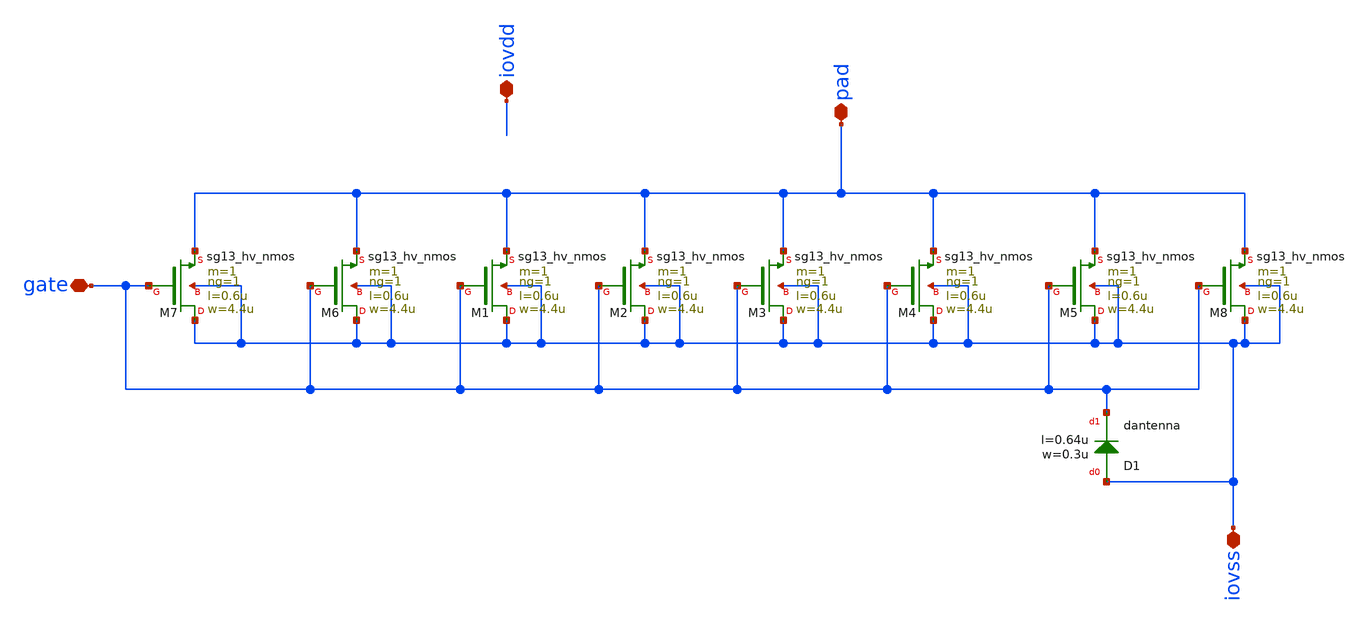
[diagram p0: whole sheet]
** sch_path: ihp-sg13g2/libs.ref/sg13g2_io/xschem/sg13g2_Clamp_N8N8D.sch
**.subckt sg13g2_Clamp_N8N8D iovss pad gate iovdd
*.iopin iovss
*.iopin pad
*.iopin gate
*.iopin iovdd
XM1 iovss gate pad iovss sg13_hv_nmos w=4.4u l=0.6u ng=1 m=1 mm_ok=1
XM2 iovss gate pad iovss sg13_hv_nmos w=4.4u l=0.6u ng=1 m=1 mm_ok=1
XM3 iovss gate pad iovss sg13_hv_nmos w=4.4u l=0.6u ng=1 m=1 mm_ok=1
XM4 iovss gate pad iovss sg13_hv_nmos w=4.4u l=0.6u ng=1 m=1 mm_ok=1
XM5 iovss gate pad iovss sg13_hv_nmos w=4.4u l=0.6u ng=1 m=1 mm_ok=1
XM6 iovss gate pad iovss sg13_hv_nmos w=4.4u l=0.6u ng=1 m=1 mm_ok=1
XM7 iovss gate pad iovss sg13_hv_nmos w=4.4u l=0.6u ng=1 m=1 mm_ok=1
XM8 iovss gate pad iovss sg13_hv_nmos w=4.4u l=0.6u ng=1 m=1 mm_ok=1
XD1 iovss gate dantenna l=0.64u w=0.3u
**.ends
.end
